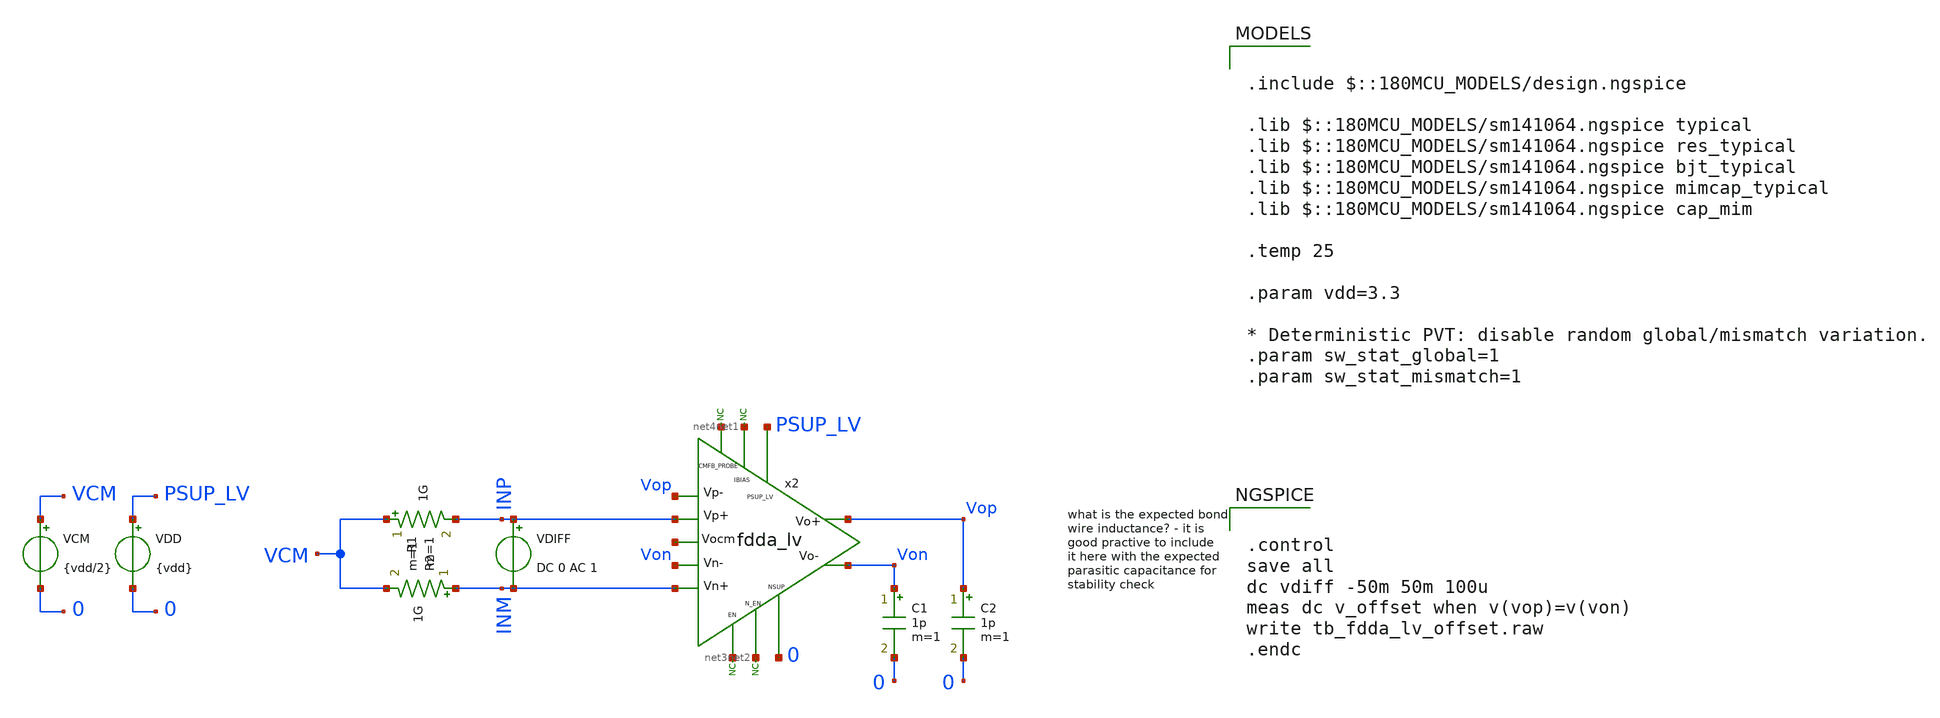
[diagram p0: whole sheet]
** sch_path: xschem/blocks/fdda_lv/tb_fdda_lv_offset.sch
**.subckt tb_fdda_lv_offset
C1 Von 0 1p m=1
x2 PSUP_LV Vop Von INM INP Vop Von net1 net2 net3 0 net4 net5 fdda_lv
* noconn #net1
* noconn #net3
* noconn #net2
VDD PSUP_LV 0 {vdd}
C2 Vop 0 1p m=1
VCM VCM 0 {vdd/2}
* noconn #net4
VDIFF INP INM DC 0 AC 1
R1 VCM INP 1G m=1
R2 INM VCM 1G m=1
**** begin user architecture code

.include $::180MCU_MODELS/design.ngspice

.lib $::180MCU_MODELS/sm141064.ngspice typical
.lib $::180MCU_MODELS/sm141064.ngspice res_typical
.lib $::180MCU_MODELS/sm141064.ngspice bjt_typical
.lib $::180MCU_MODELS/sm141064.ngspice mimcap_typical
.lib $::180MCU_MODELS/sm141064.ngspice cap_mim

.temp 25

.param vdd=3.3

* Deterministic PVT: disable random global/mismatch variation.
.param sw_stat_global=1
.param sw_stat_mismatch=1



.control
save all
dc vdiff -50m 50m 100u
meas dc v_offset when v(vop)=v(von)
write tb_fdda_lv_offset.raw
.endc


**** end user architecture code
**.ends
.end
